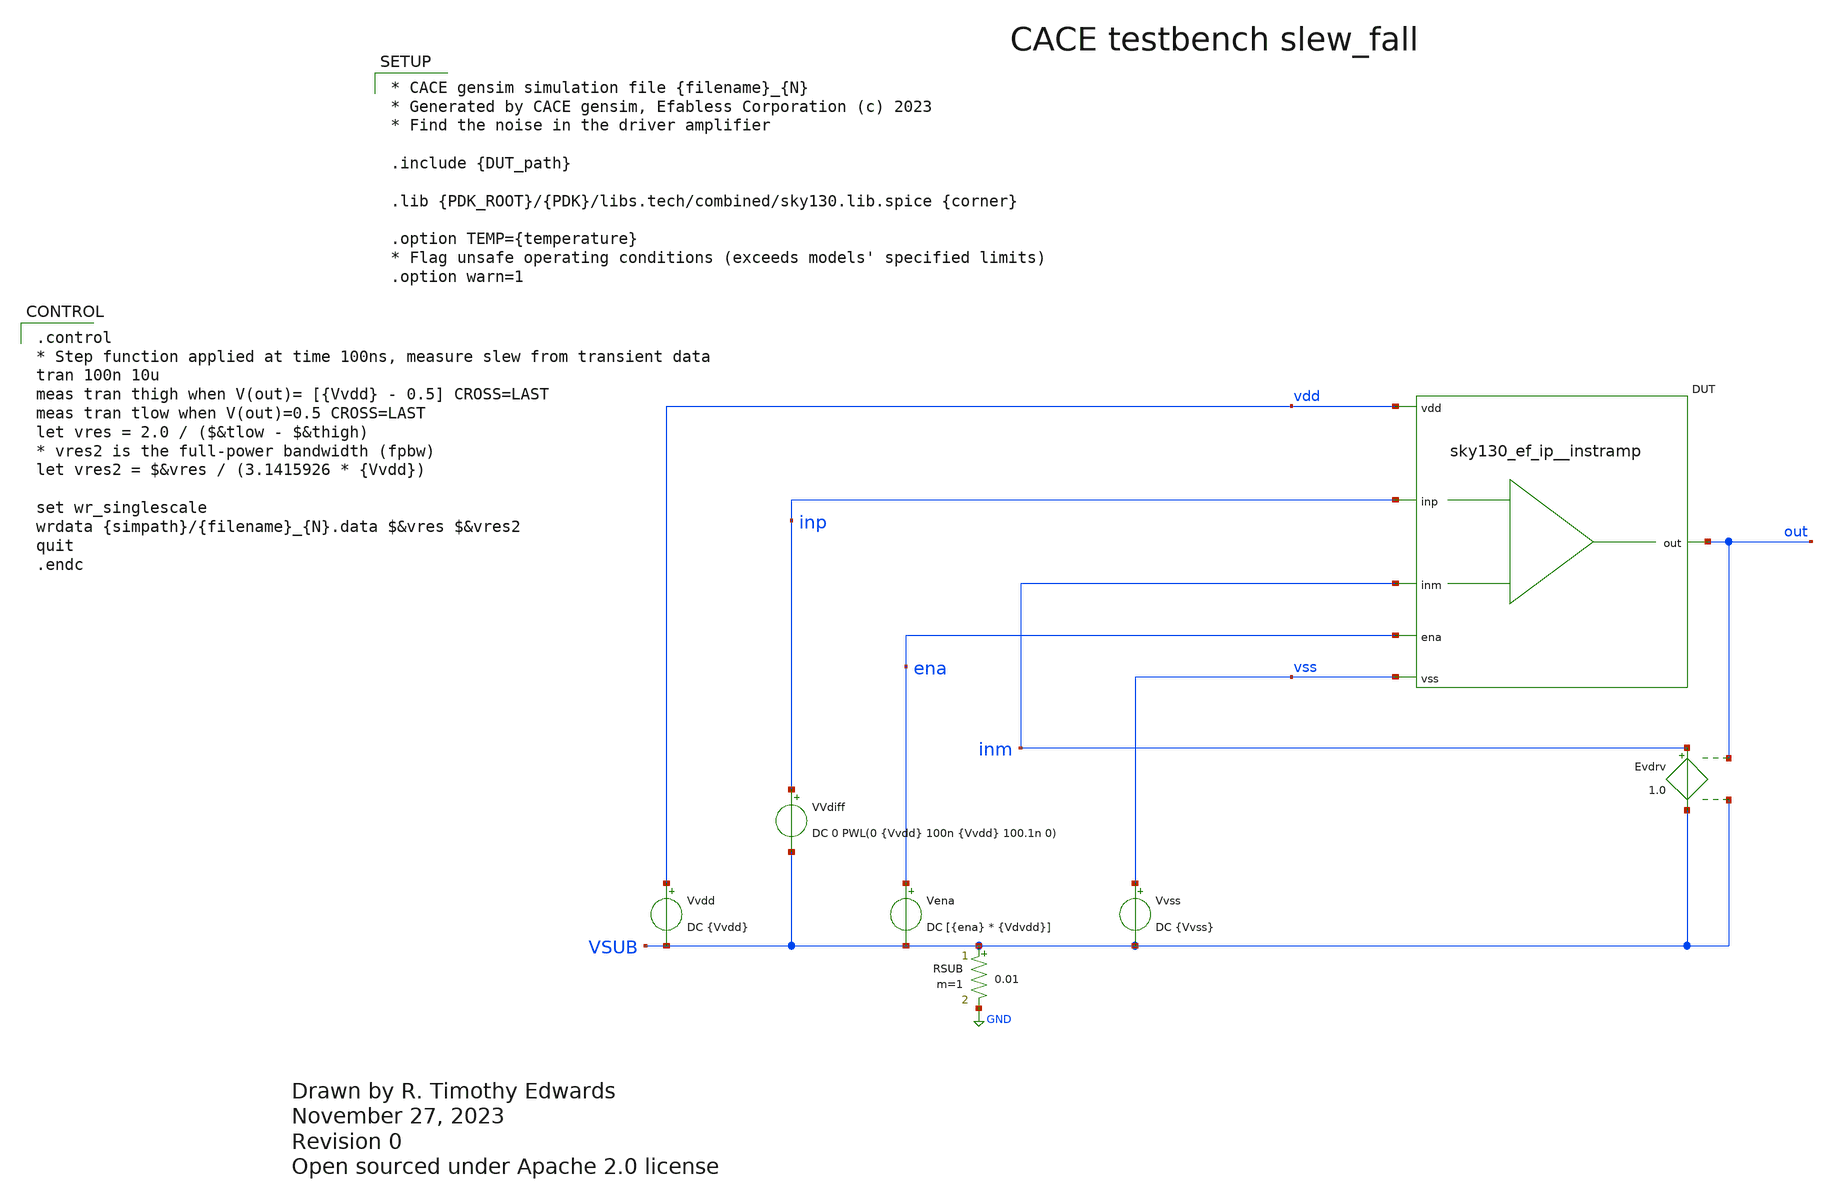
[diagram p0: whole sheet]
** sch_path: cace/slew_fall.sch
* Open sourced under Apache 2.0 license
**.subckt slew_fall
VVdiff inp VSUB DC 0 PWL(0 {Vvdd} 100n {Vvdd} 100.1n 0)
Vena ena VSUB DC [{ena} * {Vdvdd}]
Vvss vss VSUB DC {Vvss}
Vvdd vdd VSUB DC {Vvdd}
RSUB VSUB GND 0.01 m=1
XDUT {PIN|vdd|vdd} {PIN|vss|vss} {PIN|inm|inm} {PIN|inp|inp} {PIN|out|out} {PIN|ena|ena} {DUT_name}
Evdrv inm VSUB out VSUB 1.0
**** begin user architecture code

.control
* Step function applied at time 100ns, measure slew from transient data
tran 100n 10u
meas tran thigh when V(out)= [{Vvdd} - 0.5] CROSS=LAST
meas tran tlow when V(out)=0.5 CROSS=LAST
let vres = 2.0 / ($&tlow - $&thigh)
* vres2 is the full-power bandwidth (fpbw)
let vres2 = $&vres / (3.1415926 * {Vvdd})

set wr_singlescale
wrdata {simpath}/{filename}_{N}.data $&vres $&vres2
quit
.endc



* CACE gensim simulation file {filename}_{N}
* Generated by CACE gensim, Efabless Corporation (c) 2023
* Find the noise in the driver amplifier

.include {DUT_path}

.lib {PDK_ROOT}/{PDK}/libs.tech/combined/sky130.lib.spice {corner}

.option TEMP={temperature}
* Flag unsafe operating conditions (exceeds models' specified limits)
.option warn=1


**** end user architecture code
**.ends
.GLOBAL GND
.end
